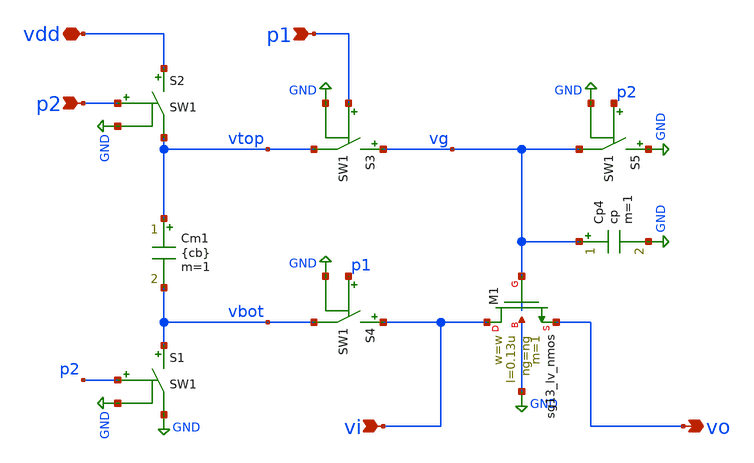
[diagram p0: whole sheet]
** sch_path: xschem/boot1.sch
**.subckt boot1 vi vo p2 p1 vdd
*.ipin vi
*.opin vo
*.ipin p2
*.ipin p1
*.iopin vdd
Cm1 vtop vbot {cb} m=1
S1 vbot GND p2 GND SW1
S2 vdd vtop p2 GND SW1
S3 vg vtop p1 GND SW1
S4 vi vbot p1 GND SW1
S5 GND vg p2 GND SW1
Cp4 vg GND cp m=1
XM1 vi vg vo GND sg13_lv_nmos w=w l=0.13u ng=ng m=1 mm_ok=1
**.ends
.GLOBAL GND
**** begin user architecture code
.MODEL SW1 SW   VT=0.6 VH=vh  RON=1 ROFF=roff
**** end user architecture code
.end
